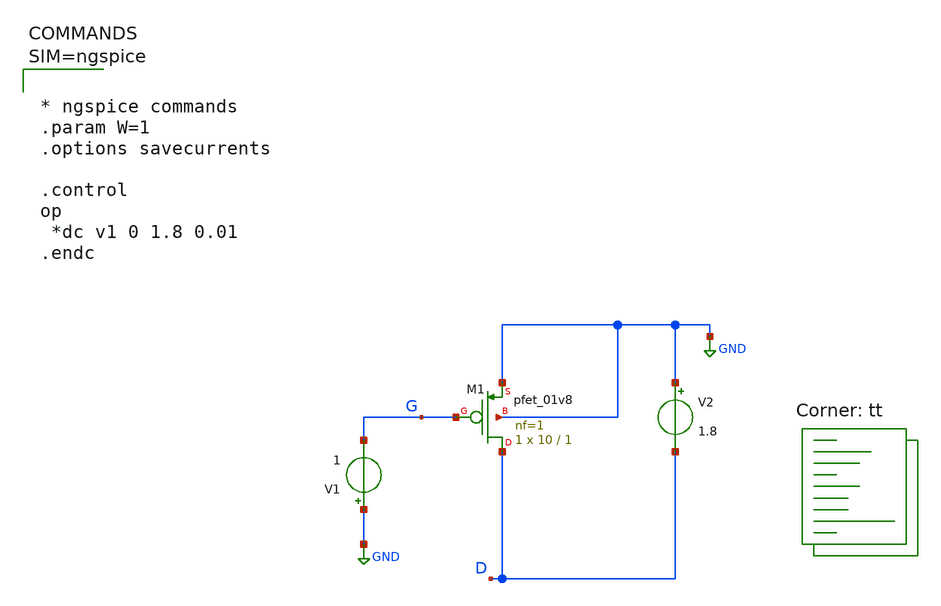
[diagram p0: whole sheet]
** sch_path: xschem/Polarizzazione_Pmos.sch
* Copyright 2021 Stefan Frederik Schippers
* Licensed under the Apache License, Version 2.0 (the "License");
* you may not use this file except in compliance with the License.
* You may obtain a copy of the License at
* https://www.apache.org/licenses/LICENSE-2.0
* Unless required by applicable law or agreed to in writing, software
* distributed under the License is distributed on an "AS IS" BASIS,
* WITHOUT WARRANTIES OR CONDITIONS OF ANY KIND, either express or implied.
* See the License for the specific language governing permissions and
* limitations under the License.
**.subckt Polarizzazione_Pmos
V1 GND G 1
V2 GND D 1.8
XM1 D G GND GND sky130_fd_pr__pfet_01v8 L=1 W=10 nf=1 ad='int((nf+1)/2) * W/nf * 0.29' as='int((nf+2)/2) * W/nf * 0.29'
+ pd='2*int((nf+1)/2) * (W/nf + 0.29)' ps='2*int((nf+2)/2) * (W/nf + 0.29)' nrd='0.29 / W' nrs='0.29 / W'
+ sa=0 sb=0 sd=0 mult=1 m=1
**** begin user architecture code
.lib $::SKYWATER_MODELS/sky130.lib.spice tt



* ngspice commands
.param W=1
.options savecurrents

.control
op
 *dc v1 0 1.8 0.01
.endc



**** end user architecture code
**.ends
.GLOBAL GND
.end
